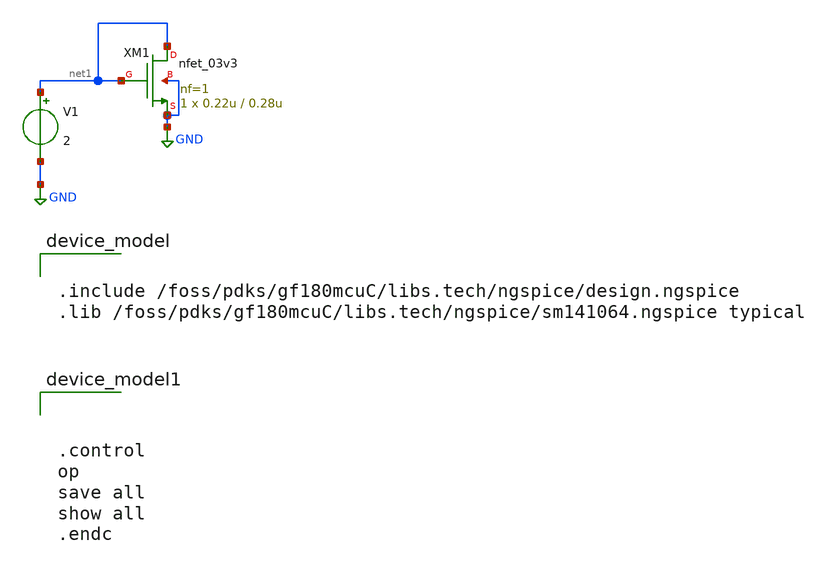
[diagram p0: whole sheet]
** sch_path: designs/examples/test.sch
**.subckt test
XM1 net1 net1 GND GND nfet_03v3 L=0.28u W=0.22u nf=1 ad='int((nf+1)/2) * W/nf * 0.18u' as='int((nf+2)/2) * W/nf * 0.18u'
+ pd='2*int((nf+1)/2) * (W/nf + 0.18u)' ps='2*int((nf+2)/2) * (W/nf + 0.18u)' nrd='0.18u / W' nrs='0.18u / W'
+ sa=0 sb=0 sd=0 m=1
V1 net1 GND 2
.save i(v1)
**** begin user architecture code


.include /foss/pdks/gf180mcuC/libs.tech/ngspice/design.ngspice
.lib /foss/pdks/gf180mcuC/libs.tech/ngspice/sm141064.ngspice typical





.control
op
save all
show all
.endc


**** end user architecture code
**.ends
.GLOBAL GND
.end
